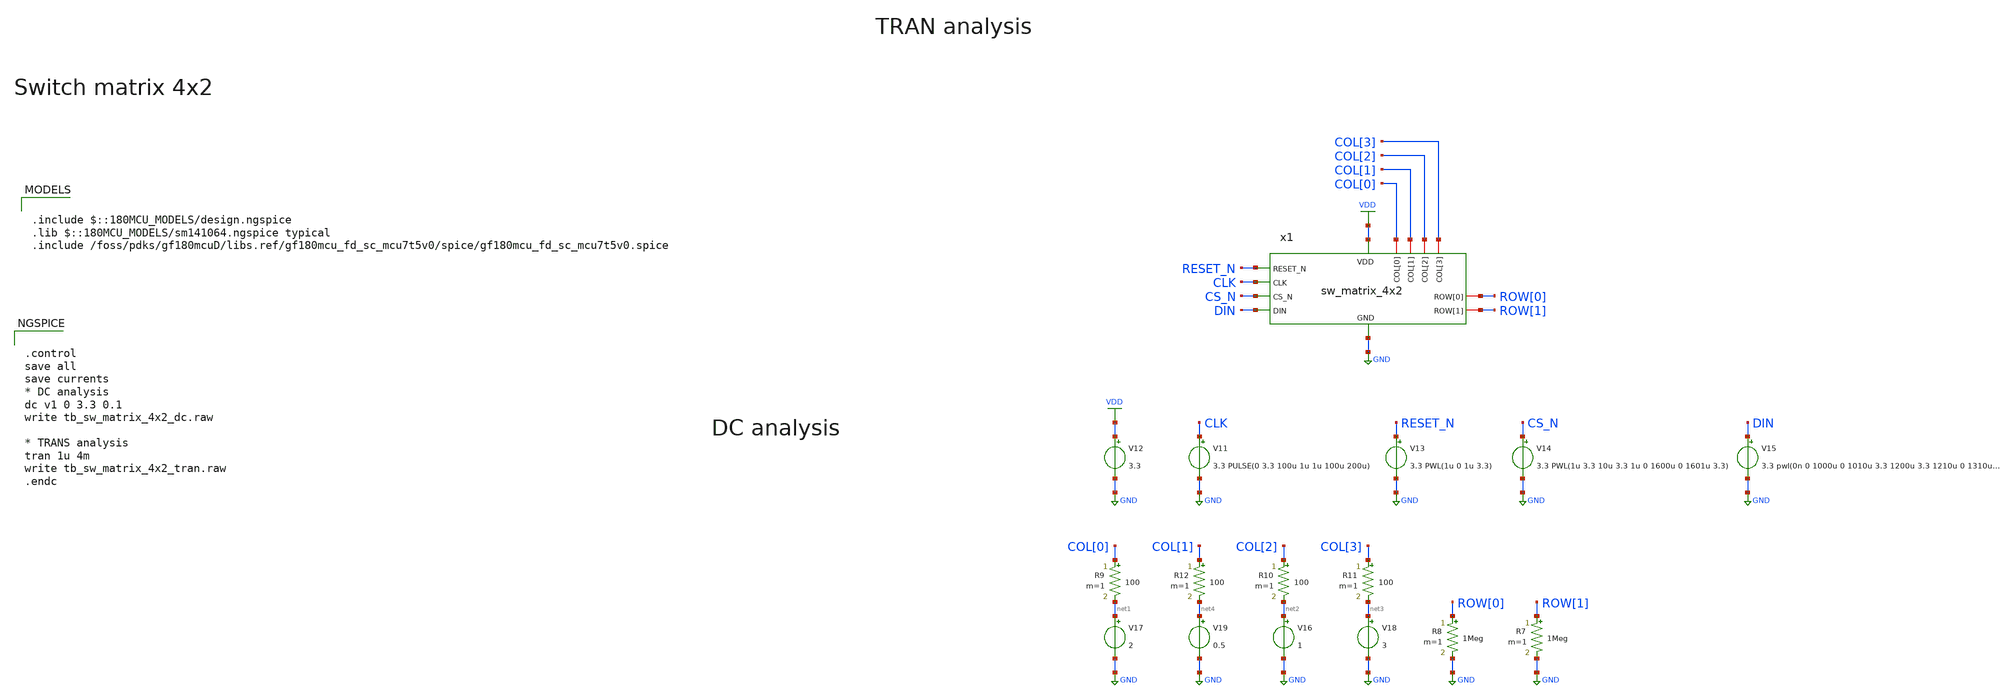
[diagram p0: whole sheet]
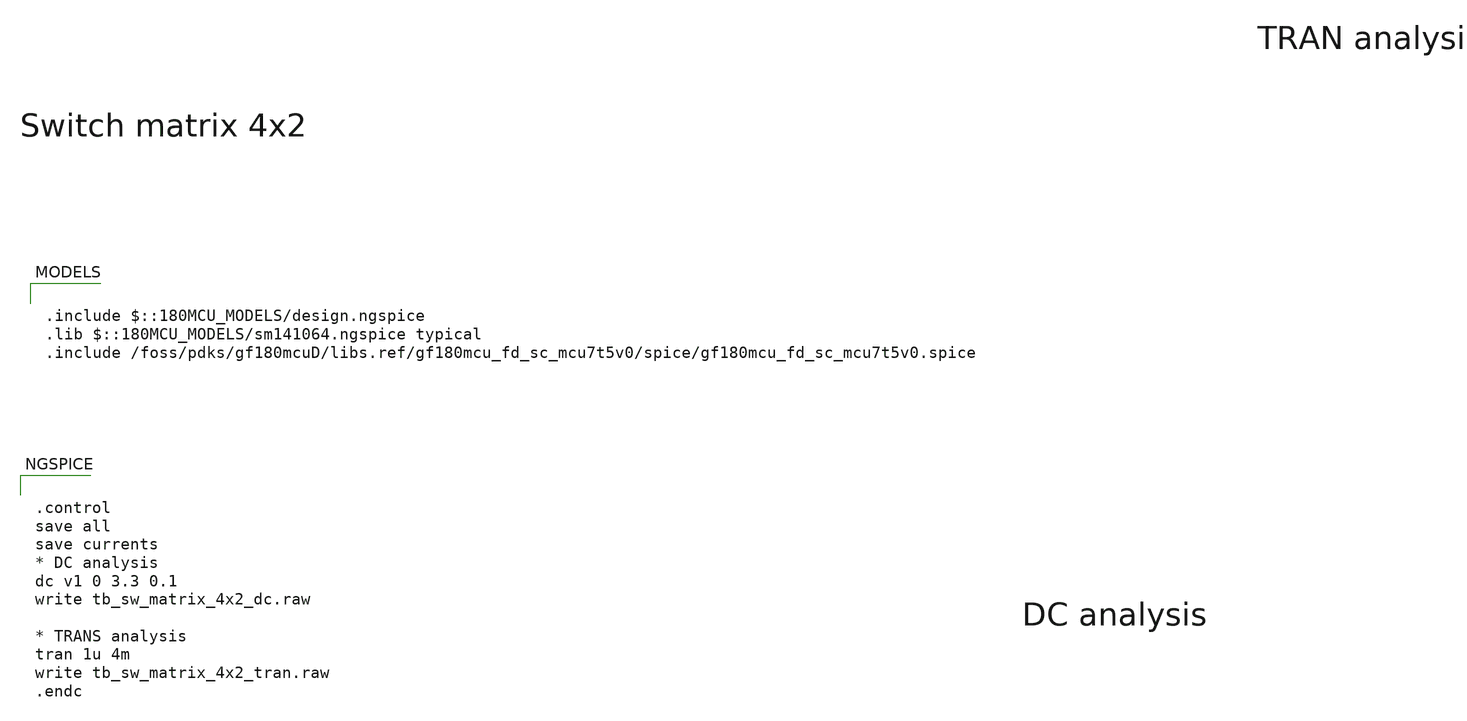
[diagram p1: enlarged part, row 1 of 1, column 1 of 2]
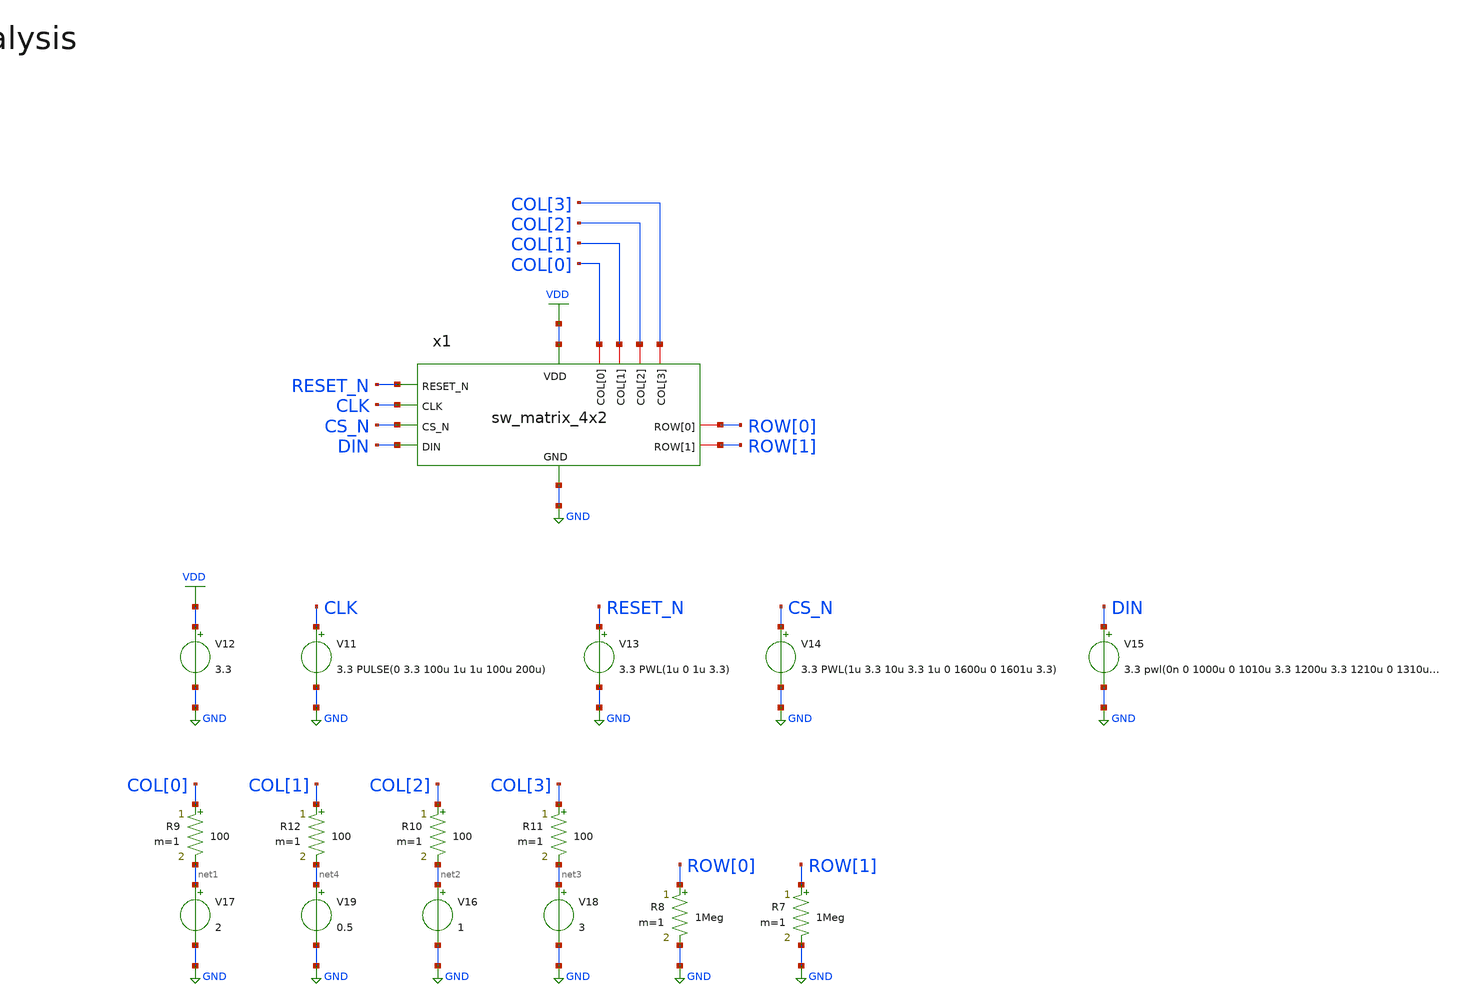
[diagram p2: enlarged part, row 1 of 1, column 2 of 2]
** sch_path: designs/libs/tb_analog/tb_sw_matrix/tb_sw_matrix_4x2.sch
* Copyright 2022 GlobalFoundries PDK Authors
* Licensed under the Apache License, Version 2.0 (the "License");
* you may not use this file except in compliance with the License.
* You may obtain a copy of the License at
* https://www.apache.org/licenses/LICENSE-2.0
* Unless required by applicable law or agreed to in writing, software
* distributed under the License is distributed on an "AS IS" BASIS,
* WITHOUT WARRANTIES OR CONDITIONS OF ANY KIND, either express or implied.
* See the License for the specific language governing permissions and
* limitations under the License.
**.subckt tb_sw_matrix_4x2
V11 CLK GND 3.3 PULSE(0 3.3 100u 1u 1u 100u 200u)
V12 VDD GND 3.3
R7 ROW[1] GND 1Meg m=1
R8 ROW[0] GND 1Meg m=1
V13 RESET_N GND 3.3 PWL(1u 0 1u 3.3)
V14 CS_N GND 3.3 PWL(1u 3.3 10u 3.3 1u 0 1600u 0 1601u 3.3)
V15 DIN GND 3.3 pwl(0n 0 1000u 0 1010u 3.3 1200u 3.3 1210u 0 1310u 0)
R9 COL[0] net1 100 m=1
R10 COL[2] net2 100 m=1
V16 net2 GND 1
V17 net1 GND 2
R11 COL[3] net3 100 m=1
V18 net3 GND 3
R12 COL[1] net4 100 m=1
V19 net4 GND 0.5
x1 VDD GND RESET_N CLK CS_N DIN COL[0] COL[1] COL[2] COL[3] ROW[0] ROW[1] sw_matrix_4x2
**** begin user architecture code

.include $::180MCU_MODELS/design.ngspice
.lib $::180MCU_MODELS/sm141064.ngspice typical
.include /foss/pdks/gf180mcuD/libs.ref/gf180mcu_fd_sc_mcu7t5v0/spice/gf180mcu_fd_sc_mcu7t5v0.spice



.control
save all
save currents
* DC analysis
dc v1 0 3.3 0.1
write tb_sw_matrix_4x2_dc.raw

* TRANS analysis
tran 1u 4m
write tb_sw_matrix_4x2_tran.raw
.endc


**** end user architecture code
**.ends
.GLOBAL GND
.GLOBAL VDD
.end
